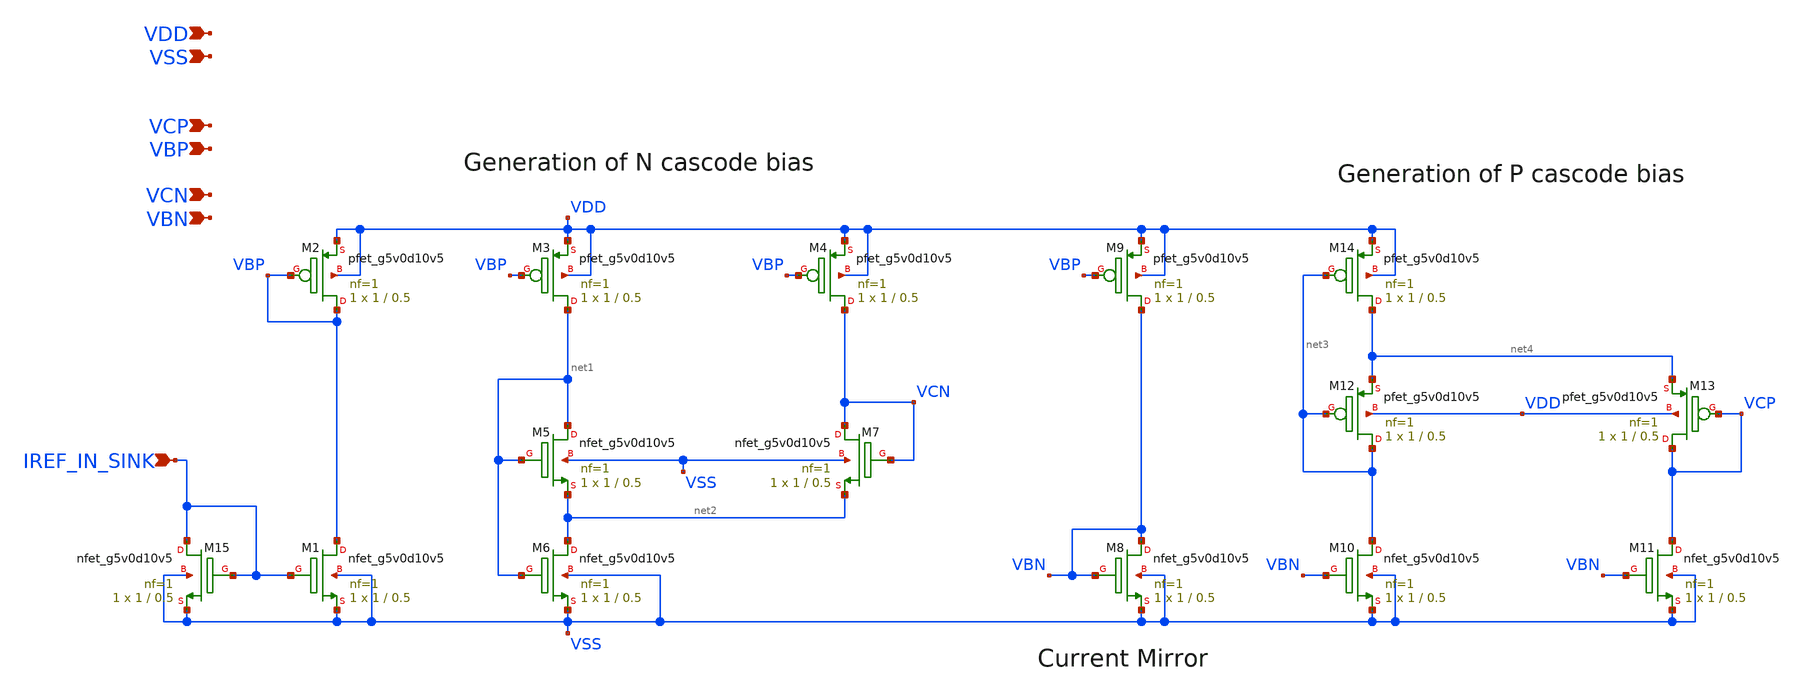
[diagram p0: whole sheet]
** sch_path: design/bias-circuit/bias_circuit.sch
**.subckt bias_circuit IREF_IN_SINK VCN VSS VDD VCP VBP VBN
*.ipin IREF_IN_SINK
*.ipin VCN
*.ipin VSS
*.ipin VDD
*.ipin VCP
*.ipin VBP
*.ipin VBN
XM2 VBP VBP VDD VDD sky130_fd_pr__pfet_g5v0d10v5 L=0.5 W=1 nf=1 ad='int((nf+1)/2) * W/nf * 0.29' as='int((nf+2)/2) * W/nf * 0.29'
+ pd='2*int((nf+1)/2) * (W/nf + 0.29)' ps='2*int((nf+2)/2) * (W/nf + 0.29)' nrd='0.29 / W' nrs='0.29 / W'
+ sa=0 sb=0 sd=0 mult=1 m=1
XM3 net1 VBP VDD VDD sky130_fd_pr__pfet_g5v0d10v5 L=0.5 W=1 nf=1 ad='int((nf+1)/2) * W/nf * 0.29' as='int((nf+2)/2) * W/nf * 0.29'
+ pd='2*int((nf+1)/2) * (W/nf + 0.29)' ps='2*int((nf+2)/2) * (W/nf + 0.29)' nrd='0.29 / W' nrs='0.29 / W'
+ sa=0 sb=0 sd=0 mult=1 m=1
XM4 VCN VBP VDD VDD sky130_fd_pr__pfet_g5v0d10v5 L=0.5 W=1 nf=1 ad='int((nf+1)/2) * W/nf * 0.29' as='int((nf+2)/2) * W/nf * 0.29'
+ pd='2*int((nf+1)/2) * (W/nf + 0.29)' ps='2*int((nf+2)/2) * (W/nf + 0.29)' nrd='0.29 / W' nrs='0.29 / W'
+ sa=0 sb=0 sd=0 mult=1 m=1
XM5 net1 net1 net2 VSS sky130_fd_pr__nfet_g5v0d10v5 L=0.5 W=1 nf=1 ad='int((nf+1)/2) * W/nf * 0.29' as='int((nf+2)/2) * W/nf * 0.29'
+ pd='2*int((nf+1)/2) * (W/nf + 0.29)' ps='2*int((nf+2)/2) * (W/nf + 0.29)' nrd='0.29 / W' nrs='0.29 / W'
+ sa=0 sb=0 sd=0 mult=1 m=1
XM6 net2 net1 VSS VSS sky130_fd_pr__nfet_g5v0d10v5 L=0.5 W=1 nf=1 ad='int((nf+1)/2) * W/nf * 0.29' as='int((nf+2)/2) * W/nf * 0.29'
+ pd='2*int((nf+1)/2) * (W/nf + 0.29)' ps='2*int((nf+2)/2) * (W/nf + 0.29)' nrd='0.29 / W' nrs='0.29 / W'
+ sa=0 sb=0 sd=0 mult=1 m=1
XM7 VCN VCN net2 VSS sky130_fd_pr__nfet_g5v0d10v5 L=0.5 W=1 nf=1 ad='int((nf+1)/2) * W/nf * 0.29' as='int((nf+2)/2) * W/nf * 0.29'
+ pd='2*int((nf+1)/2) * (W/nf + 0.29)' ps='2*int((nf+2)/2) * (W/nf + 0.29)' nrd='0.29 / W' nrs='0.29 / W'
+ sa=0 sb=0 sd=0 mult=1 m=1
XM8 VBN VBN VSS VSS sky130_fd_pr__nfet_g5v0d10v5 L=0.5 W=1 nf=1 ad='int((nf+1)/2) * W/nf * 0.29' as='int((nf+2)/2) * W/nf * 0.29'
+ pd='2*int((nf+1)/2) * (W/nf + 0.29)' ps='2*int((nf+2)/2) * (W/nf + 0.29)' nrd='0.29 / W' nrs='0.29 / W'
+ sa=0 sb=0 sd=0 mult=1 m=1
XM9 VBN VBP VDD VDD sky130_fd_pr__pfet_g5v0d10v5 L=0.5 W=1 nf=1 ad='int((nf+1)/2) * W/nf * 0.29' as='int((nf+2)/2) * W/nf * 0.29'
+ pd='2*int((nf+1)/2) * (W/nf + 0.29)' ps='2*int((nf+2)/2) * (W/nf + 0.29)' nrd='0.29 / W' nrs='0.29 / W'
+ sa=0 sb=0 sd=0 mult=1 m=1
XM10 net3 VBN VSS VSS sky130_fd_pr__nfet_g5v0d10v5 L=0.5 W=1 nf=1 ad='int((nf+1)/2) * W/nf * 0.29' as='int((nf+2)/2) * W/nf * 0.29'
+ pd='2*int((nf+1)/2) * (W/nf + 0.29)' ps='2*int((nf+2)/2) * (W/nf + 0.29)' nrd='0.29 / W' nrs='0.29 / W'
+ sa=0 sb=0 sd=0 mult=1 m=1
XM11 VCP VBN VSS VSS sky130_fd_pr__nfet_g5v0d10v5 L=0.5 W=1 nf=1 ad='int((nf+1)/2) * W/nf * 0.29' as='int((nf+2)/2) * W/nf * 0.29'
+ pd='2*int((nf+1)/2) * (W/nf + 0.29)' ps='2*int((nf+2)/2) * (W/nf + 0.29)' nrd='0.29 / W' nrs='0.29 / W'
+ sa=0 sb=0 sd=0 mult=1 m=1
XM12 net3 net3 net4 VDD sky130_fd_pr__pfet_g5v0d10v5 L=0.5 W=1 nf=1 ad='int((nf+1)/2) * W/nf * 0.29'
+ as='int((nf+2)/2) * W/nf * 0.29' pd='2*int((nf+1)/2) * (W/nf + 0.29)' ps='2*int((nf+2)/2) * (W/nf + 0.29)'
+ nrd='0.29 / W' nrs='0.29 / W' sa=0 sb=0 sd=0 mult=1 m=1
XM13 VCP VCP net4 VDD sky130_fd_pr__pfet_g5v0d10v5 L=0.5 W=1 nf=1 ad='int((nf+1)/2) * W/nf * 0.29' as='int((nf+2)/2) * W/nf * 0.29'
+ pd='2*int((nf+1)/2) * (W/nf + 0.29)' ps='2*int((nf+2)/2) * (W/nf + 0.29)' nrd='0.29 / W' nrs='0.29 / W'
+ sa=0 sb=0 sd=0 mult=1 m=1
XM14 net4 net3 VDD VDD sky130_fd_pr__pfet_g5v0d10v5 L=0.5 W=1 nf=1 ad='int((nf+1)/2) * W/nf * 0.29' as='int((nf+2)/2) * W/nf * 0.29'
+ pd='2*int((nf+1)/2) * (W/nf + 0.29)' ps='2*int((nf+2)/2) * (W/nf + 0.29)' nrd='0.29 / W' nrs='0.29 / W'
+ sa=0 sb=0 sd=0 mult=1 m=1
XM1 VBP IREF_IN_SINK VSS VSS sky130_fd_pr__nfet_g5v0d10v5 L=0.5 W=1 nf=1 ad='int((nf+1)/2) * W/nf * 0.29'
+ as='int((nf+2)/2) * W/nf * 0.29' pd='2*int((nf+1)/2) * (W/nf + 0.29)' ps='2*int((nf+2)/2) * (W/nf + 0.29)'
+ nrd='0.29 / W' nrs='0.29 / W' sa=0 sb=0 sd=0 mult=1 m=1
XM15 IREF_IN_SINK IREF_IN_SINK VSS VSS sky130_fd_pr__nfet_g5v0d10v5 L=0.5 W=1 nf=1 ad='int((nf+1)/2) * W/nf * 0.29'
+ as='int((nf+2)/2) * W/nf * 0.29' pd='2*int((nf+1)/2) * (W/nf + 0.29)' ps='2*int((nf+2)/2) * (W/nf + 0.29)'
+ nrd='0.29 / W' nrs='0.29 / W' sa=0 sb=0 sd=0 mult=1 m=1
**.ends
.end
